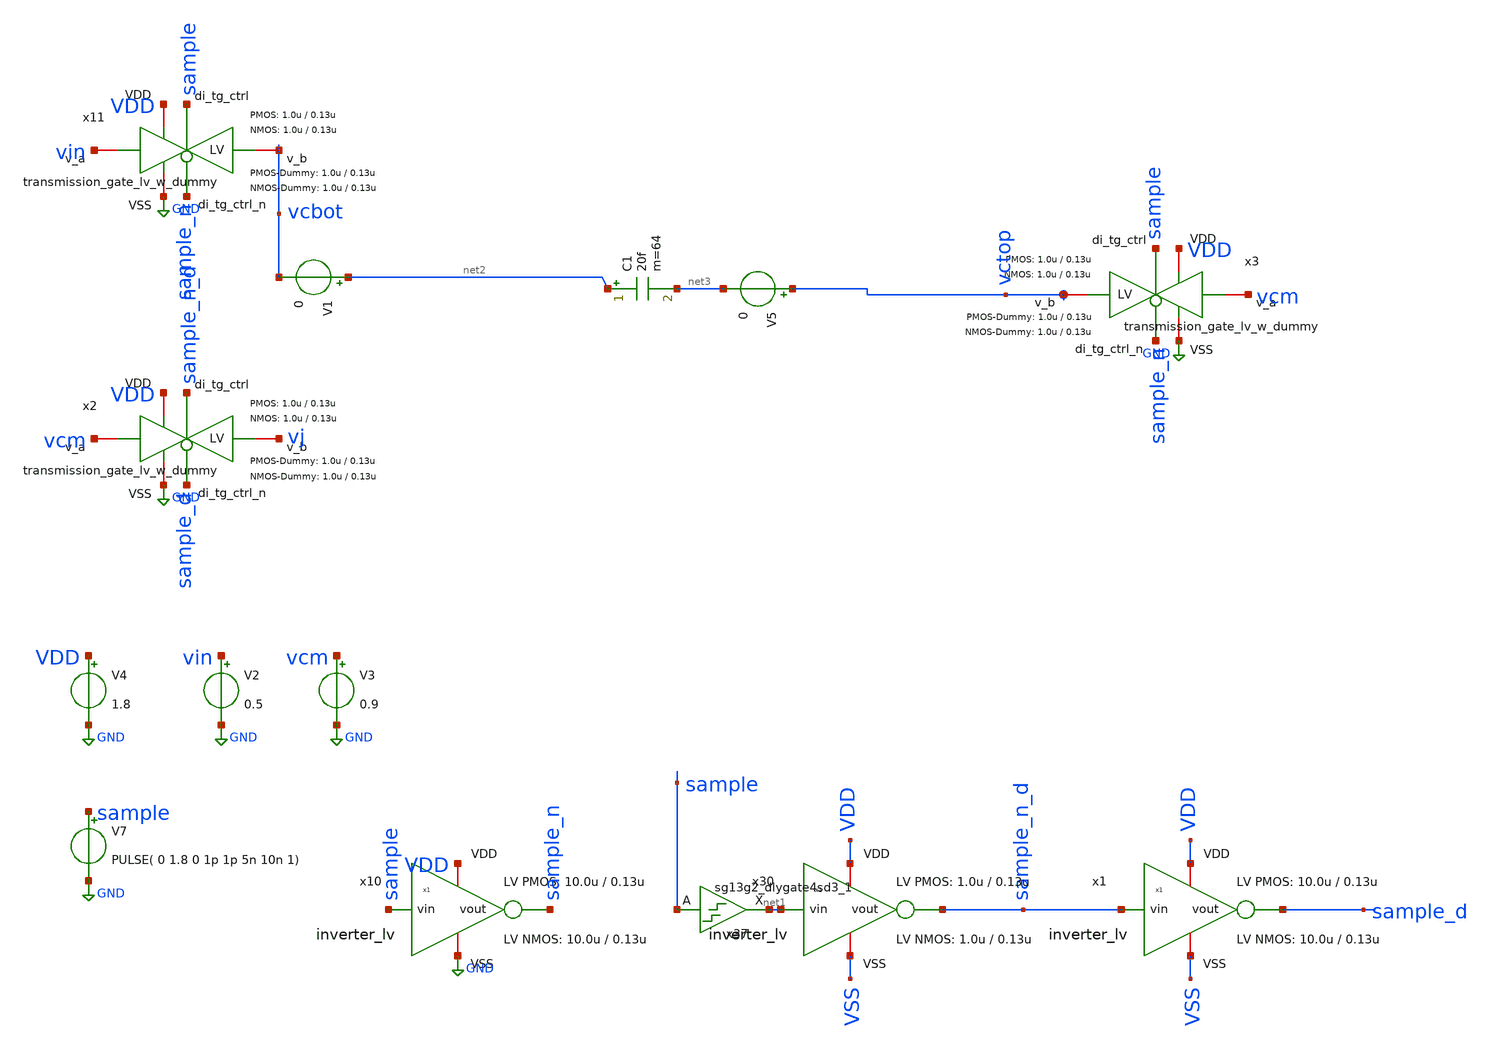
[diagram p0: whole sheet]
** sch_path: xschem/dac_icms_cell/testbenches/tb_capacitor.sch
**.subckt tb_capacitor
x11 VDD sample GND vcbot vin sample_n transmission_gate_lv_w_dummy W_P=1.0u L_P=0.13u W_N=1.0u
+ L_N=0.13u W_P_D=1.0u L_P_D=0.13u W_N_D=1.0u L_N_D=0.13u n=10
V7 sample GND PULSE( 0 1.8 0 1p 1p 5n 10n 1)
x10 VDD sample sample_n GND inverter_lv W_P=10.0u L_P=0.13u W_N=10.0u L_N=0.13u N_C=1
x1 VDD sample_n_d sample_d VSS inverter_lv W_P=10.0u L_P=0.13u W_N=10.0u L_N=0.13u N_C=1
x30 VDD net1 sample_n_d VSS inverter_lv W_P=1.0u L_P=0.13u W_N=1.0u L_N=0.13u N_C=1
x37 net1 sample VDD VSS sg13g2_dlygate4sd3_1
x2 VDD sample_n_d GND vj vcm sample_d transmission_gate_lv_w_dummy W_P=1.0u L_P=0.13u W_N=1.0u
+ L_N=0.13u W_P_D=1.0u L_P_D=0.13u W_N_D=1.0u L_N_D=0.13u n=10
V2 vin GND 0.5
V3 vcm GND 0.9
V4 VDD GND 1.8
C1 net2 net3 20f m=64
x3 VDD sample GND vctop vcm sample_n transmission_gate_lv_w_dummy W_P=1.0u L_P=0.13u W_N=1.0u
+ L_N=0.13u W_P_D=1.0u L_P_D=0.13u W_N_D=1.0u L_N_D=0.13u n=10
V1 net2 vcbot 0
V5 vctop net3 0
**** begin user architecture code


.param temp=27
.param W_P = 1.0u
.param L_P = 0.13u
.param W_N = 1.0u
.param L_N = 0.13u
.options savecurrents klu method=gear reltol=1e-2 abstol=1e-15 gmin=1e-10
.control

* Transient Analysis
tran 100p 20n

*plot {d0} {d1 + 4} {d2 + 8} {d3 + 12} {d4 + 16} {d5 + 20} {d6 + 24} {d7 + 28} {d8 + 32} {d9 + 36} {d10 + 40}
*+ {d11 + 44}
*plot {b0} {b1 + 4} {b2 + 8} {b3 + 12} {b4 + 16} {b5 + 20} {b6 + 24} {b7 + 28} {b8 + 32} {b9 + 36} {b10 + 40}
*+ {b11 + 44}
*plot {clk} {comp_in + 2} {sample + 4}
plot vctop vcbot sample
plot {vctop-vcbot} sample
plot i(v1) i(v5)
*plot x3.x14.net1-vctop x3.x18.vcap-vcbot

.endc




** IHP models
.lib cornerMOSlv.lib mos_tt
.lib cornerMOShv.lib mos_tt
.lib cornerHBT.lib hbt_typ
.lib cornerRES.lib res_typ
.include /foss/pdks/ihp-sg13g2/libs.ref/sg13g2_stdcell/spice/sg13g2_stdcell.spice


**** end user architecture code
**.ends

* expanding   symbol:  transmission_gate/transmission_gate_lv_w_dummy.sym # of pins=6
** sym_path: xschem/transmission_gate/transmission_gate_lv_w_dummy.sym
** sch_path: xschem/transmission_gate/transmission_gate_lv_w_dummy.sch
.subckt transmission_gate_lv_w_dummy VDD di_tg_ctrl VSS v_b v_a di_tg_ctrl_n  W_P=2.0u L_P=0.13u
+ W_N=2.0u L_N=0.13u W_P_D=1.0u L_P_D=0.13u W_N_D=1.0u L_N_D=0.13u n=1
*.iopin v_a
*.iopin v_b
*.iopin VDD
*.iopin VSS
*.ipin di_tg_ctrl
*.ipin di_tg_ctrl_n
XM1 v_a di_tg_ctrl v_b VSS sg13_lv_nmos w=W_N l=L_N ng=1 m=n mm_ok=1
XM2 v_a di_tg_ctrl_n v_b VDD sg13_lv_pmos w=W_P l=L_P ng=1 m=n mm_ok=1
XMdummy2 net1 di_tg_ctrl v_b VDD sg13_lv_pmos w=W_P_D l=L_P_D ng=1 m=n mm_ok=1
XMdummy1 net2 di_tg_ctrl_n v_b VSS sg13_lv_nmos w=W_N_D l=L_N_D ng=1 m=n mm_ok=1
.ends


* expanding   symbol:  inverter/inverter_lv.sym # of pins=4
** sym_path: xschem/inverter/inverter_lv.sym
** sch_path: xschem/inverter/inverter_lv.sch
.subckt inverter_lv VDD vin vout VSS  W_P=3.0u L_P=0.13u W_N=1.0u L_N=0.13u N_C=1
*.ipin vin
*.iopin VDD
*.iopin VSS
*.opin vout
XM1 vout vin VDD VDD sg13_lv_pmos w=W_P l=L_P ng=1 m={N_C} mm_ok=1
XM2 vout vin VSS VSS sg13_lv_nmos w=W_N l=L_N ng=1 m={N_C} mm_ok=1
.ends


* expanding   symbol:  sg13g2_stdcells/sg13g2_dlygate4sd3_1.sym # of pins=2
** sym_path: sg13g2_stdcells/sg13g2_dlygate4sd3_1.sym
** sch_path: sg13g2_stdcells/sg13g2_dlygate4sd3_1.sch
.subckt sg13g2_dlygate4sd3_1 X A VDD VSS
*.ipin A
*.opin X
*.iopin VDD
*.iopin VSS
XM1 net3 A VSS VSS sg13_lv_nmos w=420.00n l=130.00n ng=1 m=1 mm_ok=1
XM2 net1 net3 VSS VSS sg13_lv_nmos w=420.00n l=500.0n ng=1 m=1 mm_ok=1
XM3 net2 net1 VSS VSS sg13_lv_nmos w=420.00n l=500.0n ng=1 m=1 mm_ok=1
XM4 X net2 VSS VSS sg13_lv_nmos w=740.00n l=130.00n ng=1 m=1 mm_ok=1
XM5 net3 A VDD VDD sg13_lv_pmos w=420.00n l=130.00n ng=1 m=1 mm_ok=1
XM6 net1 net3 VDD VDD sg13_lv_pmos w=1.000u l=500.0n ng=1 m=1 mm_ok=1
XM7 net2 net1 VDD VDD sg13_lv_pmos w=1.000u l=500.0n ng=1 m=1 mm_ok=1
XM8 X net2 VDD VDD sg13_lv_pmos w=1.12u l=130.00n ng=1 m=1 mm_ok=1
.ends

.GLOBAL GND
.end
